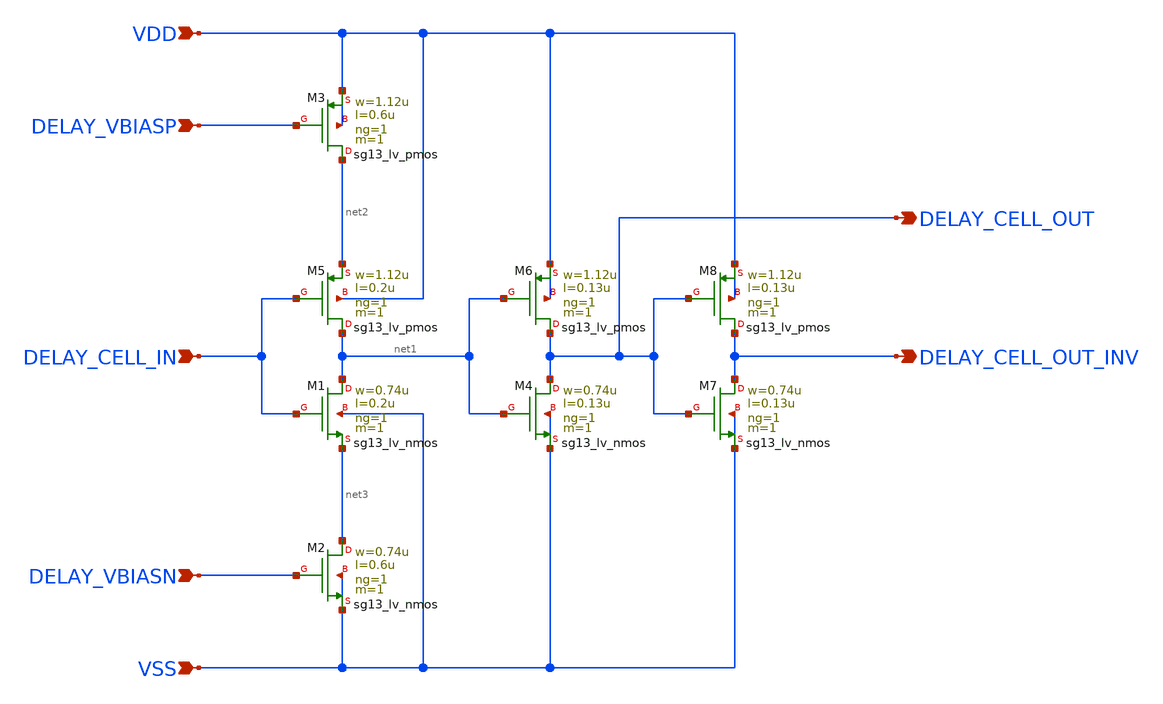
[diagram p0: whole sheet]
** sch_path: schematics/hx_delay_cell.sch
**.subckt hx_delay_cell VDD VSS DELAY_CELL_OUT_INV DELAY_VBIASN DELAY_VBIASP DELAY_CELL_IN
*+ DELAY_CELL_OUT
*.ipin VDD
*.ipin VSS
*.opin DELAY_CELL_OUT_INV
*.ipin DELAY_VBIASN
*.ipin DELAY_VBIASP
*.ipin DELAY_CELL_IN
*.opin DELAY_CELL_OUT
XM1 net1 DELAY_CELL_IN net3 VSS sg13_lv_nmos w=0.74u l=0.2u ng=1 m=1 mm_ok=1
XM2 net3 DELAY_VBIASN VSS VSS sg13_lv_nmos w=0.74u l=0.6u ng=1 m=1 mm_ok=1
XM3 net2 DELAY_VBIASP VDD VDD sg13_lv_pmos w=1.12u l=0.6u ng=1 m=1 mm_ok=1
XM4 DELAY_CELL_OUT net1 VSS VSS sg13_lv_nmos w=0.74u l=0.13u ng=1 m=1 mm_ok=1
XM5 net1 DELAY_CELL_IN net2 VDD sg13_lv_pmos w=1.12u l=0.2u ng=1 m=1 mm_ok=1
XM6 DELAY_CELL_OUT net1 VDD VDD sg13_lv_pmos w=1.12u l=0.13u ng=1 m=1 mm_ok=1
XM7 DELAY_CELL_OUT_INV DELAY_CELL_OUT VSS VSS sg13_lv_nmos w=0.74u l=0.13u ng=1 m=1 mm_ok=1
XM8 DELAY_CELL_OUT_INV DELAY_CELL_OUT VDD VDD sg13_lv_pmos w=1.12u l=0.13u ng=1 m=1 mm_ok=1
**.ends
.end
